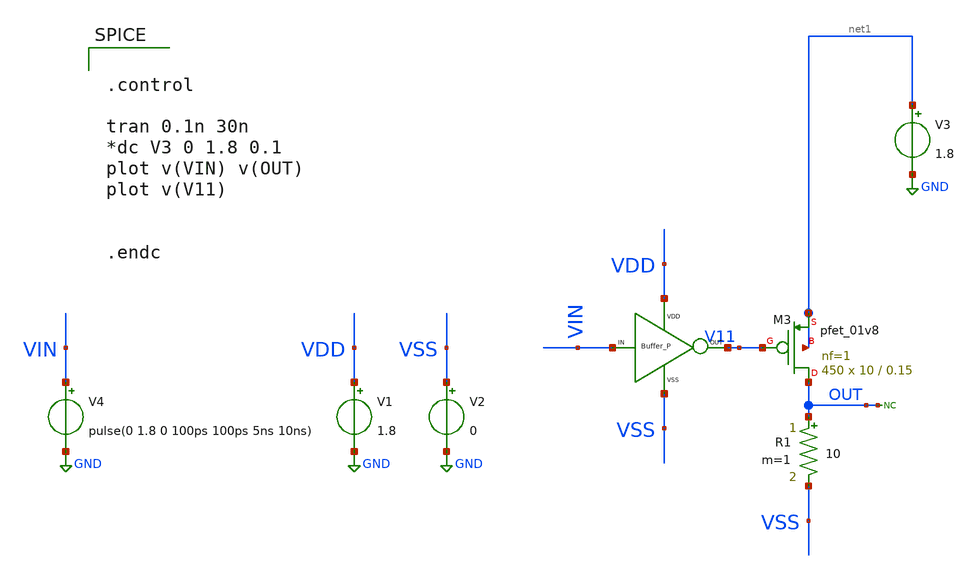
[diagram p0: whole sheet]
** sch_path: xschem/DC_DC_Converter_xschem/OTHERS/DC_DC_Converter_5/BUFFER/BUFFER_PMOS/BUFFER_P_TB.sch
**.subckt BUFFER_P_TB
V1 VDD GND 1.8
V2 VSS GND 0
* noconn OUT
V4 VIN GND pulse(0 1.8 0 100ps 100ps 5ns 10ns)
V3 net1 GND 1.8
R1 OUT VSS 10 m=1
X1 VIN V11 VDD VSS BUFFER_P
XM3 OUT V11 net1 net1 sky130_fd_pr__pfet_01v8 L=0.15 W=10 nf=1 ad='int((nf+1)/2) * W/nf * 0.29' as='int((nf+2)/2) * W/nf * 0.29'
+ pd='2*int((nf+1)/2) * (W/nf + 0.29)' ps='2*int((nf+2)/2) * (W/nf + 0.29)' nrd='0.29 / W' nrs='0.29 / W'
+ sa=0 sb=0 sd=0 mult=450 m=450
**** begin user architecture code

** opencircuitdesign pdks install
.lib $::SKYWATER_MODELS/sky130.lib.spice tt




.control

tran 0.1n 30n
*dc V3 0 1.8 0.1
plot v(VIN) v(OUT)
plot v(V11)


.endc


**** end user architecture code
**.ends
.GLOBAL GND
.end
